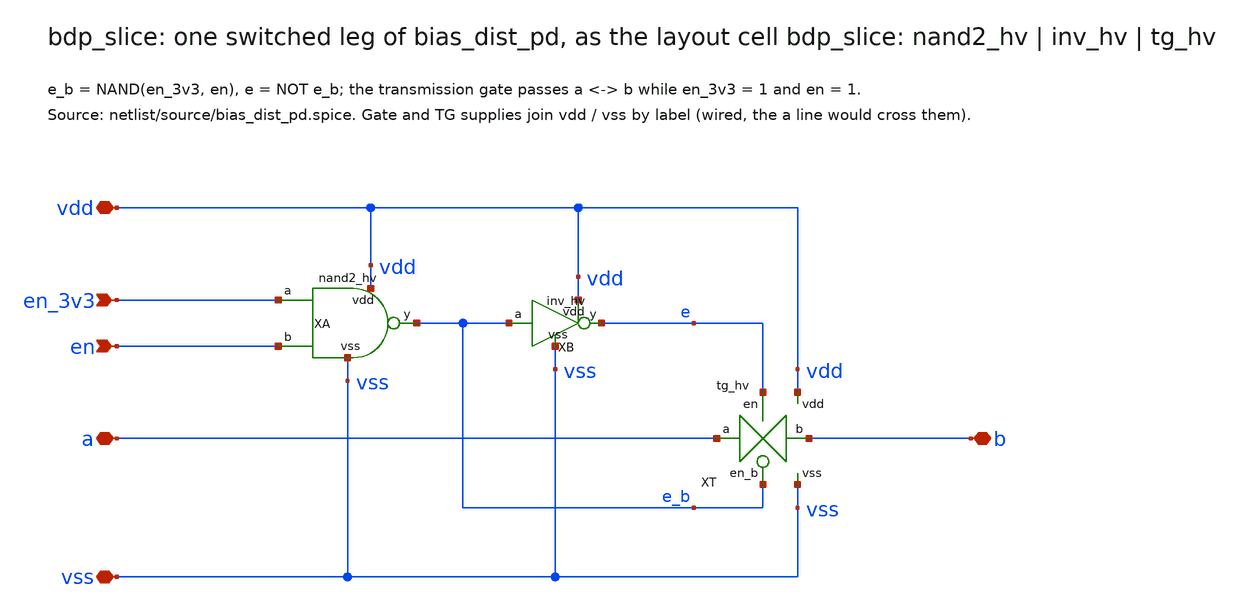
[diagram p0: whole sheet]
** sch_path: macros/bias_dist_pd/schematic/xschem/bdp_slice.sch
**.subckt bdp_slice vdd vss en_3v3 en a b
*.iopin vdd
*.iopin vss
*.ipin en_3v3
*.ipin en
*.iopin a
*.iopin b
XA vdd vss en_3v3 en e_b nand2_hv
XB vdd vss e_b e inv_hv
XT vdd vss e e_b a b tg_hv
**.ends

* expanding   symbol:  nand2_hv.sym # of pins=5
** sym_path: macros/hv_logic/schematic/xschem/nand2_hv.sym
** sch_path: macros/hv_logic/schematic/xschem/nand2_hv.sch
.subckt nand2_hv vdd vss a b y
*.iopin vdd
*.iopin vss
*.ipin a
*.ipin b
*.opin y
XPA y a vdd vdd sg13_hv_pmos w=1u l=0.45u ng=1 m=1 mm_ok=1
XPB y b vdd vdd sg13_hv_pmos w=1u l=0.45u ng=1 m=1 mm_ok=1
XNA y a n1 vss sg13_hv_nmos w=1u l=0.45u ng=1 m=1 mm_ok=1
XNB n1 b vss vss sg13_hv_nmos w=1u l=0.45u ng=1 m=1 mm_ok=1
.ends


* expanding   symbol:  inv_hv.sym # of pins=4
** sym_path: macros/hv_logic/schematic/xschem/inv_hv.sym
** sch_path: macros/hv_logic/schematic/xschem/inv_hv.sch
.subckt inv_hv vdd vss a y
*.iopin vdd
*.iopin vss
*.ipin a
*.opin y
XP y a vdd vdd sg13_hv_pmos w=1u l=0.45u ng=1 m=1 mm_ok=1
XN y a vss vss sg13_hv_nmos w=1u l=0.45u ng=1 m=1 mm_ok=1
.ends


* expanding   symbol:  tg_hv.sym # of pins=6
** sym_path: macros/hv_logic/schematic/xschem/tg_hv.sym
** sch_path: macros/hv_logic/schematic/xschem/tg_hv.sch
.subckt tg_hv vdd vss en en_b a b
*.iopin vdd
*.iopin vss
*.ipin en
*.ipin en_b
*.iopin a
*.iopin b
XN a en b vss sg13_hv_nmos w=1u l=0.45u ng=1 m=1 mm_ok=1
XP a en_b b vdd sg13_hv_pmos w=1u l=0.45u ng=1 m=1 mm_ok=1
.ends

.end
